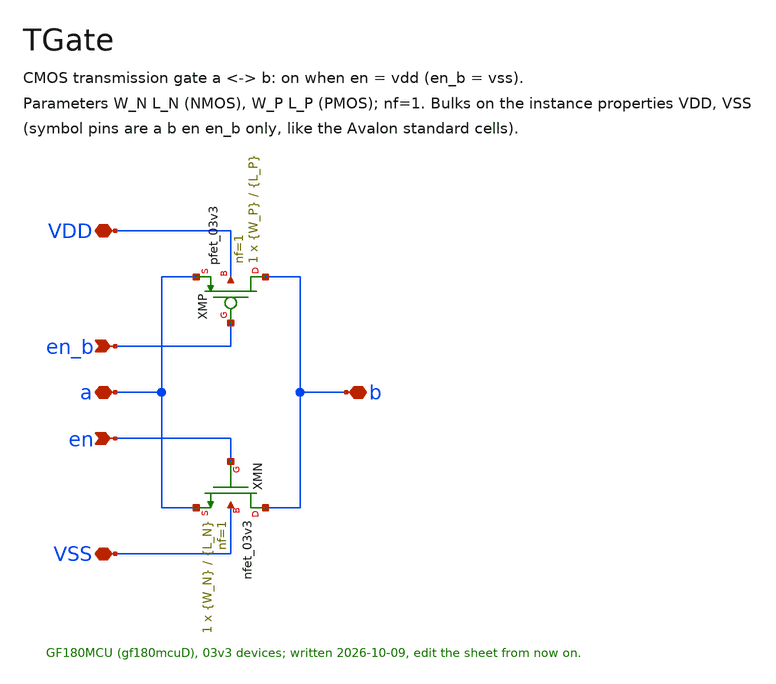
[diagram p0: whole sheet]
** sch_path: macros/PadEnable/schematic/xschem/TGate.sch
**.subckt TGate a b en_b en VDD VSS
*.iopin a
*.iopin b
*.ipin en_b
*.ipin en
*.iopin VDD
*.iopin VSS
XMP b en_b a VDD pfet_03v3 L={L_P} W={W_P} nf=1 ad='int((nf+1)/2) * W/nf * 0.18u' as='int((nf+2)/2) * W/nf * 0.18u'
+ pd='2*int((nf+1)/2) * (W/nf + 0.18u)' ps='2*int((nf+2)/2) * (W/nf + 0.18u)' nrd='0.18u / W' nrs='0.18u / W'
+ sa=0 sb=0 sd=0 m=1
XMN b en a VSS nfet_03v3 L={L_N} W={W_N} nf=1 ad='int((nf+1)/2) * W/nf * 0.18u' as='int((nf+2)/2) * W/nf * 0.18u'
+ pd='2*int((nf+1)/2) * (W/nf + 0.18u)' ps='2*int((nf+2)/2) * (W/nf + 0.18u)' nrd='0.18u / W' nrs='0.18u / W'
+ sa=0 sb=0 sd=0 m=1
**.ends
.end
